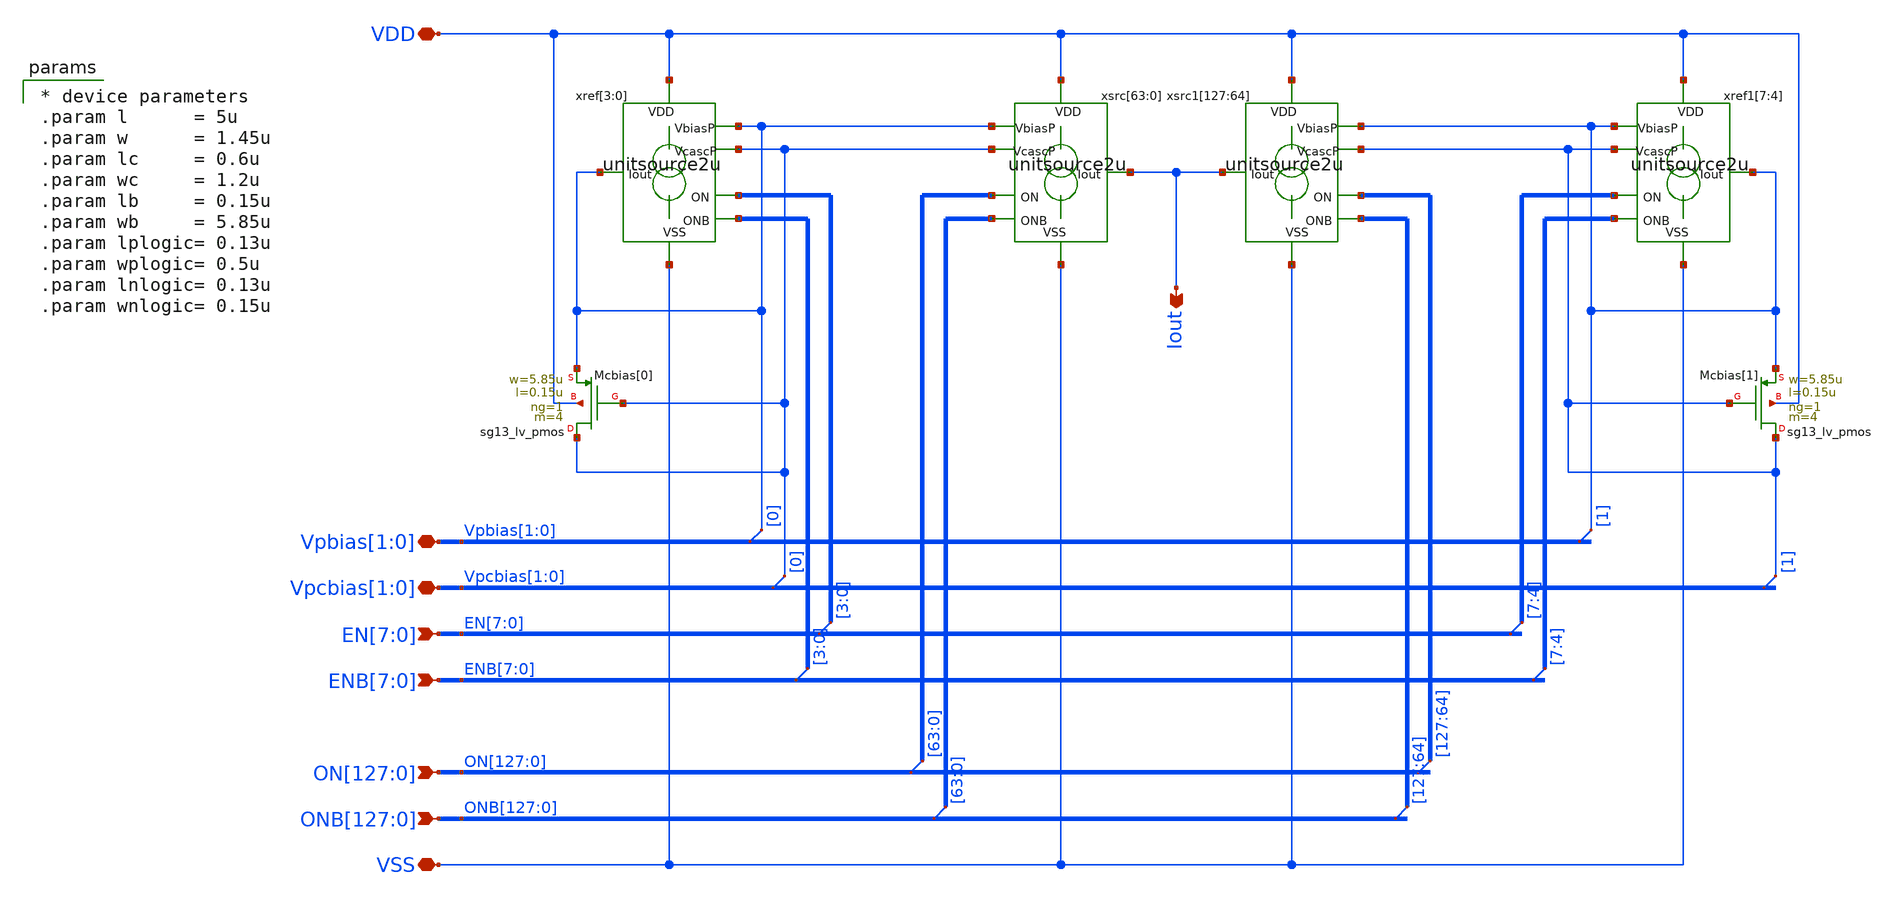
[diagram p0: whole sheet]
** sch_path: xschem/dac128module.sch
**.subckt dac128module Iout
*+ ON[127],ON[126],ON[125],ON[124],ON[123],ON[122],ON[121],ON[120],ON[119],ON[118],ON[117],ON[116],ON[115],ON[114],ON[113],ON[112],ON[111],ON[110],ON[109],ON[108],ON[107],ON[106],ON[105],ON[104],ON[103],ON[102],ON[101],ON[100],ON[99],ON[98],ON[97],ON[96],ON[95],ON[94],ON[93],ON[92],ON[91],ON[90],ON[89],ON[88],ON[87],ON[86],ON[85],ON[84],ON[83],ON[82],ON[81],ON[80],ON[79],ON[78],ON[77],ON[76],ON[75],ON[74],ON[73],ON[72],ON[71],ON[70],ON[69],ON[68],ON[67],ON[66],ON[65],ON[64],ON[63],ON[62],ON[61],ON[60],ON[59],ON[58],ON[57],ON[56],ON[55],ON[54],ON[53],ON[52],ON[51],ON[50],ON[49],ON[48],ON[47],ON[46],ON[45],ON[44],ON[43],ON[42],ON[41],ON[40],ON[39],ON[38],ON[37],ON[36],ON[35],ON[34],ON[33],ON[32],ON[31],ON[30],ON[29],ON[28],ON[27],ON[26],ON[25],ON[24],ON[23],ON[22],ON[21],ON[20],ON[19],ON[18],ON[17],ON[16],ON[15],ON[14],ON[13],ON[12],ON[11],ON[10],ON[9],ON[8],ON[7],ON[6],ON[5],ON[4],ON[3],ON[2],ON[1],ON[0]
*+ ONB[127],ONB[126],ONB[125],ONB[124],ONB[123],ONB[122],ONB[121],ONB[120],ONB[119],ONB[118],ONB[117],ONB[116],ONB[115],ONB[114],ONB[113],ONB[112],ONB[111],ONB[110],ONB[109],ONB[108],ONB[107],ONB[106],ONB[105],ONB[104],ONB[103],ONB[102],ONB[101],ONB[100],ONB[99],ONB[98],ONB[97],ONB[96],ONB[95],ONB[94],ONB[93],ONB[92],ONB[91],ONB[90],ONB[89],ONB[88],ONB[87],ONB[86],ONB[85],ONB[84],ONB[83],ONB[82],ONB[81],ONB[80],ONB[79],ONB[78],ONB[77],ONB[76],ONB[75],ONB[74],ONB[73],ONB[72],ONB[71],ONB[70],ONB[69],ONB[68],ONB[67],ONB[66],ONB[65],ONB[64],ONB[63],ONB[62],ONB[61],ONB[60],ONB[59],ONB[58],ONB[57],ONB[56],ONB[55],ONB[54],ONB[53],ONB[52],ONB[51],ONB[50],ONB[49],ONB[48],ONB[47],ONB[46],ONB[45],ONB[44],ONB[43],ONB[42],ONB[41],ONB[40],ONB[39],ONB[38],ONB[37],ONB[36],ONB[35],ONB[34],ONB[33],ONB[32],ONB[31],ONB[30],ONB[29],ONB[28],ONB[27],ONB[26],ONB[25],ONB[24],ONB[23],ONB[22],ONB[21],ONB[20],ONB[19],ONB[18],ONB[17],ONB[16],ONB[15],ONB[14],ONB[13],ONB[12],ONB[11],ONB[10],ONB[9],ONB[8],ONB[7],ONB[6],ONB[5],ONB[4],ONB[3],ONB[2],ONB[1],ONB[0] VSS VDD Vpcbias[1],Vpcbias[0] EN[7],EN[6],EN[5],EN[4],EN[3],EN[2],EN[1],EN[0]
*+ ENB[7],ENB[6],ENB[5],ENB[4],ENB[3],ENB[2],ENB[1],ENB[0] Vpbias[1],Vpbias[0]
*.opin Iout
*.ipin
*+ ON[127],ON[126],ON[125],ON[124],ON[123],ON[122],ON[121],ON[120],ON[119],ON[118],ON[117],ON[116],ON[115],ON[114],ON[113],ON[112],ON[111],ON[110],ON[109],ON[108],ON[107],ON[106],ON[105],ON[104],ON[103],ON[102],ON[101],ON[100],ON[99],ON[98],ON[97],ON[96],ON[95],ON[94],ON[93],ON[92],ON[91],ON[90],ON[89],ON[88],ON[87],ON[86],ON[85],ON[84],ON[83],ON[82],ON[81],ON[80],ON[79],ON[78],ON[77],ON[76],ON[75],ON[74],ON[73],ON[72],ON[71],ON[70],ON[69],ON[68],ON[67],ON[66],ON[65],ON[64],ON[63],ON[62],ON[61],ON[60],ON[59],ON[58],ON[57],ON[56],ON[55],ON[54],ON[53],ON[52],ON[51],ON[50],ON[49],ON[48],ON[47],ON[46],ON[45],ON[44],ON[43],ON[42],ON[41],ON[40],ON[39],ON[38],ON[37],ON[36],ON[35],ON[34],ON[33],ON[32],ON[31],ON[30],ON[29],ON[28],ON[27],ON[26],ON[25],ON[24],ON[23],ON[22],ON[21],ON[20],ON[19],ON[18],ON[17],ON[16],ON[15],ON[14],ON[13],ON[12],ON[11],ON[10],ON[9],ON[8],ON[7],ON[6],ON[5],ON[4],ON[3],ON[2],ON[1],ON[0]
*.ipin
*+ ONB[127],ONB[126],ONB[125],ONB[124],ONB[123],ONB[122],ONB[121],ONB[120],ONB[119],ONB[118],ONB[117],ONB[116],ONB[115],ONB[114],ONB[113],ONB[112],ONB[111],ONB[110],ONB[109],ONB[108],ONB[107],ONB[106],ONB[105],ONB[104],ONB[103],ONB[102],ONB[101],ONB[100],ONB[99],ONB[98],ONB[97],ONB[96],ONB[95],ONB[94],ONB[93],ONB[92],ONB[91],ONB[90],ONB[89],ONB[88],ONB[87],ONB[86],ONB[85],ONB[84],ONB[83],ONB[82],ONB[81],ONB[80],ONB[79],ONB[78],ONB[77],ONB[76],ONB[75],ONB[74],ONB[73],ONB[72],ONB[71],ONB[70],ONB[69],ONB[68],ONB[67],ONB[66],ONB[65],ONB[64],ONB[63],ONB[62],ONB[61],ONB[60],ONB[59],ONB[58],ONB[57],ONB[56],ONB[55],ONB[54],ONB[53],ONB[52],ONB[51],ONB[50],ONB[49],ONB[48],ONB[47],ONB[46],ONB[45],ONB[44],ONB[43],ONB[42],ONB[41],ONB[40],ONB[39],ONB[38],ONB[37],ONB[36],ONB[35],ONB[34],ONB[33],ONB[32],ONB[31],ONB[30],ONB[29],ONB[28],ONB[27],ONB[26],ONB[25],ONB[24],ONB[23],ONB[22],ONB[21],ONB[20],ONB[19],ONB[18],ONB[17],ONB[16],ONB[15],ONB[14],ONB[13],ONB[12],ONB[11],ONB[10],ONB[9],ONB[8],ONB[7],ONB[6],ONB[5],ONB[4],ONB[3],ONB[2],ONB[1],ONB[0]
*.iopin VSS
*.iopin VDD
*.iopin Vpcbias[1],Vpcbias[0]
*.ipin EN[7],EN[6],EN[5],EN[4],EN[3],EN[2],EN[1],EN[0]
*.ipin ENB[7],ENB[6],ENB[5],ENB[4],ENB[3],ENB[2],ENB[1],ENB[0]
*.iopin Vpbias[1],Vpbias[0]
XMcbias[0] Vpcbias[0] Vpcbias[0] Vpbias[0] VDD sg13_lv_pmos w=5.85u l=0.15u ng=1 m=4 mm_ok=1
xref[3] VDD Vpbias[0] EN[3] ENB[3] Vpbias[0] Vpcbias[0] VSS unitsource2u
xref[2] VDD Vpbias[0] EN[2] ENB[2] Vpbias[0] Vpcbias[0] VSS unitsource2u
xref[1] VDD Vpbias[0] EN[1] ENB[1] Vpbias[0] Vpcbias[0] VSS unitsource2u
xref[0] VDD Vpbias[0] EN[0] ENB[0] Vpbias[0] Vpcbias[0] VSS unitsource2u
xsrc[63] VDD Vpbias[0] ON[63] ONB[63] Iout Vpcbias[0] VSS unitsource2u
xsrc[62] VDD Vpbias[0] ON[62] ONB[62] Iout Vpcbias[0] VSS unitsource2u
xsrc[61] VDD Vpbias[0] ON[61] ONB[61] Iout Vpcbias[0] VSS unitsource2u
xsrc[60] VDD Vpbias[0] ON[60] ONB[60] Iout Vpcbias[0] VSS unitsource2u
xsrc[59] VDD Vpbias[0] ON[59] ONB[59] Iout Vpcbias[0] VSS unitsource2u
xsrc[58] VDD Vpbias[0] ON[58] ONB[58] Iout Vpcbias[0] VSS unitsource2u
xsrc[57] VDD Vpbias[0] ON[57] ONB[57] Iout Vpcbias[0] VSS unitsource2u
xsrc[56] VDD Vpbias[0] ON[56] ONB[56] Iout Vpcbias[0] VSS unitsource2u
xsrc[55] VDD Vpbias[0] ON[55] ONB[55] Iout Vpcbias[0] VSS unitsource2u
xsrc[54] VDD Vpbias[0] ON[54] ONB[54] Iout Vpcbias[0] VSS unitsource2u
xsrc[53] VDD Vpbias[0] ON[53] ONB[53] Iout Vpcbias[0] VSS unitsource2u
xsrc[52] VDD Vpbias[0] ON[52] ONB[52] Iout Vpcbias[0] VSS unitsource2u
xsrc[51] VDD Vpbias[0] ON[51] ONB[51] Iout Vpcbias[0] VSS unitsource2u
xsrc[50] VDD Vpbias[0] ON[50] ONB[50] Iout Vpcbias[0] VSS unitsource2u
xsrc[49] VDD Vpbias[0] ON[49] ONB[49] Iout Vpcbias[0] VSS unitsource2u
xsrc[48] VDD Vpbias[0] ON[48] ONB[48] Iout Vpcbias[0] VSS unitsource2u
xsrc[47] VDD Vpbias[0] ON[47] ONB[47] Iout Vpcbias[0] VSS unitsource2u
xsrc[46] VDD Vpbias[0] ON[46] ONB[46] Iout Vpcbias[0] VSS unitsource2u
xsrc[45] VDD Vpbias[0] ON[45] ONB[45] Iout Vpcbias[0] VSS unitsource2u
xsrc[44] VDD Vpbias[0] ON[44] ONB[44] Iout Vpcbias[0] VSS unitsource2u
xsrc[43] VDD Vpbias[0] ON[43] ONB[43] Iout Vpcbias[0] VSS unitsource2u
xsrc[42] VDD Vpbias[0] ON[42] ONB[42] Iout Vpcbias[0] VSS unitsource2u
xsrc[41] VDD Vpbias[0] ON[41] ONB[41] Iout Vpcbias[0] VSS unitsource2u
xsrc[40] VDD Vpbias[0] ON[40] ONB[40] Iout Vpcbias[0] VSS unitsource2u
xsrc[39] VDD Vpbias[0] ON[39] ONB[39] Iout Vpcbias[0] VSS unitsource2u
xsrc[38] VDD Vpbias[0] ON[38] ONB[38] Iout Vpcbias[0] VSS unitsource2u
xsrc[37] VDD Vpbias[0] ON[37] ONB[37] Iout Vpcbias[0] VSS unitsource2u
xsrc[36] VDD Vpbias[0] ON[36] ONB[36] Iout Vpcbias[0] VSS unitsource2u
xsrc[35] VDD Vpbias[0] ON[35] ONB[35] Iout Vpcbias[0] VSS unitsource2u
xsrc[34] VDD Vpbias[0] ON[34] ONB[34] Iout Vpcbias[0] VSS unitsource2u
xsrc[33] VDD Vpbias[0] ON[33] ONB[33] Iout Vpcbias[0] VSS unitsource2u
xsrc[32] VDD Vpbias[0] ON[32] ONB[32] Iout Vpcbias[0] VSS unitsource2u
xsrc[31] VDD Vpbias[0] ON[31] ONB[31] Iout Vpcbias[0] VSS unitsource2u
xsrc[30] VDD Vpbias[0] ON[30] ONB[30] Iout Vpcbias[0] VSS unitsource2u
xsrc[29] VDD Vpbias[0] ON[29] ONB[29] Iout Vpcbias[0] VSS unitsource2u
xsrc[28] VDD Vpbias[0] ON[28] ONB[28] Iout Vpcbias[0] VSS unitsource2u
xsrc[27] VDD Vpbias[0] ON[27] ONB[27] Iout Vpcbias[0] VSS unitsource2u
xsrc[26] VDD Vpbias[0] ON[26] ONB[26] Iout Vpcbias[0] VSS unitsource2u
xsrc[25] VDD Vpbias[0] ON[25] ONB[25] Iout Vpcbias[0] VSS unitsource2u
xsrc[24] VDD Vpbias[0] ON[24] ONB[24] Iout Vpcbias[0] VSS unitsource2u
xsrc[23] VDD Vpbias[0] ON[23] ONB[23] Iout Vpcbias[0] VSS unitsource2u
xsrc[22] VDD Vpbias[0] ON[22] ONB[22] Iout Vpcbias[0] VSS unitsource2u
xsrc[21] VDD Vpbias[0] ON[21] ONB[21] Iout Vpcbias[0] VSS unitsource2u
xsrc[20] VDD Vpbias[0] ON[20] ONB[20] Iout Vpcbias[0] VSS unitsource2u
xsrc[19] VDD Vpbias[0] ON[19] ONB[19] Iout Vpcbias[0] VSS unitsource2u
xsrc[18] VDD Vpbias[0] ON[18] ONB[18] Iout Vpcbias[0] VSS unitsource2u
xsrc[17] VDD Vpbias[0] ON[17] ONB[17] Iout Vpcbias[0] VSS unitsource2u
xsrc[16] VDD Vpbias[0] ON[16] ONB[16] Iout Vpcbias[0] VSS unitsource2u
xsrc[15] VDD Vpbias[0] ON[15] ONB[15] Iout Vpcbias[0] VSS unitsource2u
xsrc[14] VDD Vpbias[0] ON[14] ONB[14] Iout Vpcbias[0] VSS unitsource2u
xsrc[13] VDD Vpbias[0] ON[13] ONB[13] Iout Vpcbias[0] VSS unitsource2u
xsrc[12] VDD Vpbias[0] ON[12] ONB[12] Iout Vpcbias[0] VSS unitsource2u
xsrc[11] VDD Vpbias[0] ON[11] ONB[11] Iout Vpcbias[0] VSS unitsource2u
xsrc[10] VDD Vpbias[0] ON[10] ONB[10] Iout Vpcbias[0] VSS unitsource2u
xsrc[9] VDD Vpbias[0] ON[9] ONB[9] Iout Vpcbias[0] VSS unitsource2u
xsrc[8] VDD Vpbias[0] ON[8] ONB[8] Iout Vpcbias[0] VSS unitsource2u
xsrc[7] VDD Vpbias[0] ON[7] ONB[7] Iout Vpcbias[0] VSS unitsource2u
xsrc[6] VDD Vpbias[0] ON[6] ONB[6] Iout Vpcbias[0] VSS unitsource2u
xsrc[5] VDD Vpbias[0] ON[5] ONB[5] Iout Vpcbias[0] VSS unitsource2u
xsrc[4] VDD Vpbias[0] ON[4] ONB[4] Iout Vpcbias[0] VSS unitsource2u
xsrc[3] VDD Vpbias[0] ON[3] ONB[3] Iout Vpcbias[0] VSS unitsource2u
xsrc[2] VDD Vpbias[0] ON[2] ONB[2] Iout Vpcbias[0] VSS unitsource2u
xsrc[1] VDD Vpbias[0] ON[1] ONB[1] Iout Vpcbias[0] VSS unitsource2u
xsrc[0] VDD Vpbias[0] ON[0] ONB[0] Iout Vpcbias[0] VSS unitsource2u
XMcbias[1] Vpcbias[1] Vpcbias[1] Vpbias[1] VDD sg13_lv_pmos w=5.85u l=0.15u ng=1 m=4 mm_ok=1
xref1[7] VDD Vpbias[1] EN[7] ENB[7] Vpbias[1] Vpcbias[1] VSS unitsource2u
xref1[6] VDD Vpbias[1] EN[6] ENB[6] Vpbias[1] Vpcbias[1] VSS unitsource2u
xref1[5] VDD Vpbias[1] EN[5] ENB[5] Vpbias[1] Vpcbias[1] VSS unitsource2u
xref1[4] VDD Vpbias[1] EN[4] ENB[4] Vpbias[1] Vpcbias[1] VSS unitsource2u
xsrc1[127] VDD Vpbias[1] ON[127] ONB[127] Iout Vpcbias[1] VSS unitsource2u
xsrc1[126] VDD Vpbias[1] ON[126] ONB[126] Iout Vpcbias[1] VSS unitsource2u
xsrc1[125] VDD Vpbias[1] ON[125] ONB[125] Iout Vpcbias[1] VSS unitsource2u
xsrc1[124] VDD Vpbias[1] ON[124] ONB[124] Iout Vpcbias[1] VSS unitsource2u
xsrc1[123] VDD Vpbias[1] ON[123] ONB[123] Iout Vpcbias[1] VSS unitsource2u
xsrc1[122] VDD Vpbias[1] ON[122] ONB[122] Iout Vpcbias[1] VSS unitsource2u
xsrc1[121] VDD Vpbias[1] ON[121] ONB[121] Iout Vpcbias[1] VSS unitsource2u
xsrc1[120] VDD Vpbias[1] ON[120] ONB[120] Iout Vpcbias[1] VSS unitsource2u
xsrc1[119] VDD Vpbias[1] ON[119] ONB[119] Iout Vpcbias[1] VSS unitsource2u
xsrc1[118] VDD Vpbias[1] ON[118] ONB[118] Iout Vpcbias[1] VSS unitsource2u
xsrc1[117] VDD Vpbias[1] ON[117] ONB[117] Iout Vpcbias[1] VSS unitsource2u
xsrc1[116] VDD Vpbias[1] ON[116] ONB[116] Iout Vpcbias[1] VSS unitsource2u
xsrc1[115] VDD Vpbias[1] ON[115] ONB[115] Iout Vpcbias[1] VSS unitsource2u
xsrc1[114] VDD Vpbias[1] ON[114] ONB[114] Iout Vpcbias[1] VSS unitsource2u
xsrc1[113] VDD Vpbias[1] ON[113] ONB[113] Iout Vpcbias[1] VSS unitsource2u
xsrc1[112] VDD Vpbias[1] ON[112] ONB[112] Iout Vpcbias[1] VSS unitsource2u
xsrc1[111] VDD Vpbias[1] ON[111] ONB[111] Iout Vpcbias[1] VSS unitsource2u
xsrc1[110] VDD Vpbias[1] ON[110] ONB[110] Iout Vpcbias[1] VSS unitsource2u
xsrc1[109] VDD Vpbias[1] ON[109] ONB[109] Iout Vpcbias[1] VSS unitsource2u
xsrc1[108] VDD Vpbias[1] ON[108] ONB[108] Iout Vpcbias[1] VSS unitsource2u
xsrc1[107] VDD Vpbias[1] ON[107] ONB[107] Iout Vpcbias[1] VSS unitsource2u
xsrc1[106] VDD Vpbias[1] ON[106] ONB[106] Iout Vpcbias[1] VSS unitsource2u
xsrc1[105] VDD Vpbias[1] ON[105] ONB[105] Iout Vpcbias[1] VSS unitsource2u
xsrc1[104] VDD Vpbias[1] ON[104] ONB[104] Iout Vpcbias[1] VSS unitsource2u
xsrc1[103] VDD Vpbias[1] ON[103] ONB[103] Iout Vpcbias[1] VSS unitsource2u
xsrc1[102] VDD Vpbias[1] ON[102] ONB[102] Iout Vpcbias[1] VSS unitsource2u
xsrc1[101] VDD Vpbias[1] ON[101] ONB[101] Iout Vpcbias[1] VSS unitsource2u
xsrc1[100] VDD Vpbias[1] ON[100] ONB[100] Iout Vpcbias[1] VSS unitsource2u
xsrc1[99] VDD Vpbias[1] ON[99] ONB[99] Iout Vpcbias[1] VSS unitsource2u
xsrc1[98] VDD Vpbias[1] ON[98] ONB[98] Iout Vpcbias[1] VSS unitsource2u
xsrc1[97] VDD Vpbias[1] ON[97] ONB[97] Iout Vpcbias[1] VSS unitsource2u
xsrc1[96] VDD Vpbias[1] ON[96] ONB[96] Iout Vpcbias[1] VSS unitsource2u
xsrc1[95] VDD Vpbias[1] ON[95] ONB[95] Iout Vpcbias[1] VSS unitsource2u
xsrc1[94] VDD Vpbias[1] ON[94] ONB[94] Iout Vpcbias[1] VSS unitsource2u
xsrc1[93] VDD Vpbias[1] ON[93] ONB[93] Iout Vpcbias[1] VSS unitsource2u
xsrc1[92] VDD Vpbias[1] ON[92] ONB[92] Iout Vpcbias[1] VSS unitsource2u
xsrc1[91] VDD Vpbias[1] ON[91] ONB[91] Iout Vpcbias[1] VSS unitsource2u
xsrc1[90] VDD Vpbias[1] ON[90] ONB[90] Iout Vpcbias[1] VSS unitsource2u
xsrc1[89] VDD Vpbias[1] ON[89] ONB[89] Iout Vpcbias[1] VSS unitsource2u
xsrc1[88] VDD Vpbias[1] ON[88] ONB[88] Iout Vpcbias[1] VSS unitsource2u
xsrc1[87] VDD Vpbias[1] ON[87] ONB[87] Iout Vpcbias[1] VSS unitsource2u
xsrc1[86] VDD Vpbias[1] ON[86] ONB[86] Iout Vpcbias[1] VSS unitsource2u
xsrc1[85] VDD Vpbias[1] ON[85] ONB[85] Iout Vpcbias[1] VSS unitsource2u
xsrc1[84] VDD Vpbias[1] ON[84] ONB[84] Iout Vpcbias[1] VSS unitsource2u
xsrc1[83] VDD Vpbias[1] ON[83] ONB[83] Iout Vpcbias[1] VSS unitsource2u
xsrc1[82] VDD Vpbias[1] ON[82] ONB[82] Iout Vpcbias[1] VSS unitsource2u
xsrc1[81] VDD Vpbias[1] ON[81] ONB[81] Iout Vpcbias[1] VSS unitsource2u
xsrc1[80] VDD Vpbias[1] ON[80] ONB[80] Iout Vpcbias[1] VSS unitsource2u
xsrc1[79] VDD Vpbias[1] ON[79] ONB[79] Iout Vpcbias[1] VSS unitsource2u
xsrc1[78] VDD Vpbias[1] ON[78] ONB[78] Iout Vpcbias[1] VSS unitsource2u
xsrc1[77] VDD Vpbias[1] ON[77] ONB[77] Iout Vpcbias[1] VSS unitsource2u
xsrc1[76] VDD Vpbias[1] ON[76] ONB[76] Iout Vpcbias[1] VSS unitsource2u
xsrc1[75] VDD Vpbias[1] ON[75] ONB[75] Iout Vpcbias[1] VSS unitsource2u
xsrc1[74] VDD Vpbias[1] ON[74] ONB[74] Iout Vpcbias[1] VSS unitsource2u
xsrc1[73] VDD Vpbias[1] ON[73] ONB[73] Iout Vpcbias[1] VSS unitsource2u
xsrc1[72] VDD Vpbias[1] ON[72] ONB[72] Iout Vpcbias[1] VSS unitsource2u
xsrc1[71] VDD Vpbias[1] ON[71] ONB[71] Iout Vpcbias[1] VSS unitsource2u
xsrc1[70] VDD Vpbias[1] ON[70] ONB[70] Iout Vpcbias[1] VSS unitsource2u
xsrc1[69] VDD Vpbias[1] ON[69] ONB[69] Iout Vpcbias[1] VSS unitsource2u
xsrc1[68] VDD Vpbias[1] ON[68] ONB[68] Iout Vpcbias[1] VSS unitsource2u
xsrc1[67] VDD Vpbias[1] ON[67] ONB[67] Iout Vpcbias[1] VSS unitsource2u
xsrc1[66] VDD Vpbias[1] ON[66] ONB[66] Iout Vpcbias[1] VSS unitsource2u
xsrc1[65] VDD Vpbias[1] ON[65] ONB[65] Iout Vpcbias[1] VSS unitsource2u
xsrc1[64] VDD Vpbias[1] ON[64] ONB[64] Iout Vpcbias[1] VSS unitsource2u
* tap: EN[7:0] --> EN[3:0]
* tap: ENB[7:0] --> ENB[3:0]
* tap: ENB[7:0] --> ENB[7:4]
* tap: EN[7:0] --> EN[7:4]
* tap: ON[127:0] --> ON[63:0]
* tap: ONB[127:0] --> ONB[63:0]
* tap: ON[127:0] --> ON[127:64]
* tap: ONB[127:0] --> ONB[127:64]
* tap: Vpbias[1:0] --> Vpbias[0]
* tap: Vpcbias[1:0] --> Vpcbias[0]
* tap: Vpbias[1:0] --> Vpbias[1]
* tap: Vpcbias[1:0] --> Vpcbias[1]
**** begin user architecture code

* device parameters
.param l      = 5u
.param w      = 1.45u
.param lc     = 0.6u
.param wc     = 1.2u
.param lb     = 0.15u
.param wb     = 5.85u
.param lplogic= 0.13u
.param wplogic= 0.5u
.param lnlogic= 0.13u
.param wnlogic= 0.15u


**** end user architecture code
**.ends

* expanding   symbol:  unitsource2u.sym # of pins=7
** sym_path: xschem/unitsource2u.sym
** sch_path: xschem/unitsource2u.sch
.subckt unitsource2u VDD VbiasP ON ONB Iout VcascP VSS
*.iopin VSS
*.iopin VDD
*.iopin VbiasP
*.iopin VcascP
*.ipin ON
*.ipin ONB
*.iopin Iout
xnonoverlap VDD VSS ON ONB on_n off_n nonoverlap
xsw VDD off_n Vcasc on_n VcascP cascodeswitch_pmos
xsrc VDD VbiasP Vcasc Iout pcsource2u
.ends


* expanding   symbol:  nonoverlap.sym # of pins=6
** sym_path: xschem/nonoverlap.sym
** sch_path: xschem/nonoverlap.sch
.subckt nonoverlap VDD VSS INP INN OUTN OUTP
*.iopin VSS
*.iopin VDD
*.ipin INP
*.ipin INN
*.opin OUTP
*.opin OUTN
XM1 OUTN INP VDD VDD sg13_lv_pmos w=0.3u l=0.13u ng=1 m=1 mm_ok=1
XM2 OUTP INN VDD VDD sg13_lv_pmos w=0.3u l=0.13u ng=1 m=1 mm_ok=1
XM3 OUTN OUTP VSS VSS sg13_lv_nmos w=0.15u l=0.52u ng=1 m=1 mm_ok=1
XM4 OUTP OUTN VSS VSS sg13_lv_nmos w=0.15u l=0.52u ng=1 m=1 mm_ok=1
.ends


* expanding   symbol:  cascodeswitch_pmos.sym # of pins=5
** sym_path: xschem/cascodeswitch_pmos.sym
** sch_path: xschem/cascodeswitch_pmos.sch
.subckt cascodeswitch_pmos VDD off_n Vcasc on_n Vbpcasc
*.ipin off_n
*.ipin Vbpcasc
*.opin Vcasc
*.ipin on_n
*.ipin VDD
XMpullup Vcasc off_n VDD VDD sg13_lv_pmos w=0.3u l=0.13u ng=1 m=1 mm_ok=1
XMbias Vbpcasc on_n Vcasc VDD sg13_lv_pmos w=0.3u l=0.13u ng=1 m=1 mm_ok=1
.ends


* expanding   symbol:  pcsource2u.sym # of pins=4
** sym_path: xschem/pcsource2u.sym
** sch_path: xschem/pcsource2u.sch
.subckt pcsource2u VDD VbiasP VcascodeP Iout
*.ipin VcascodeP
*.ipin VbiasP
*.opin Iout
*.ipin VDD
XMsrc drain net4 VDD net1 sg13_lv_pmos w=1.45u l=5u ng=1 m=1 mm_ok=1
XMcasc Iout net3 drain net2 sg13_lv_pmos w=1.2u l=0.6u ng=1 m=1 mm_ok=1
Vgsrc net4 VbiasP 0
.save i(vgsrc)
Vgcasc net3 VcascodeP 0
.save i(vgcasc)
Vbsrc VDD net1 0
.save i(vbsrc)
Vbcasc VDD net2 0
.save i(vbcasc)
.ends

.end
